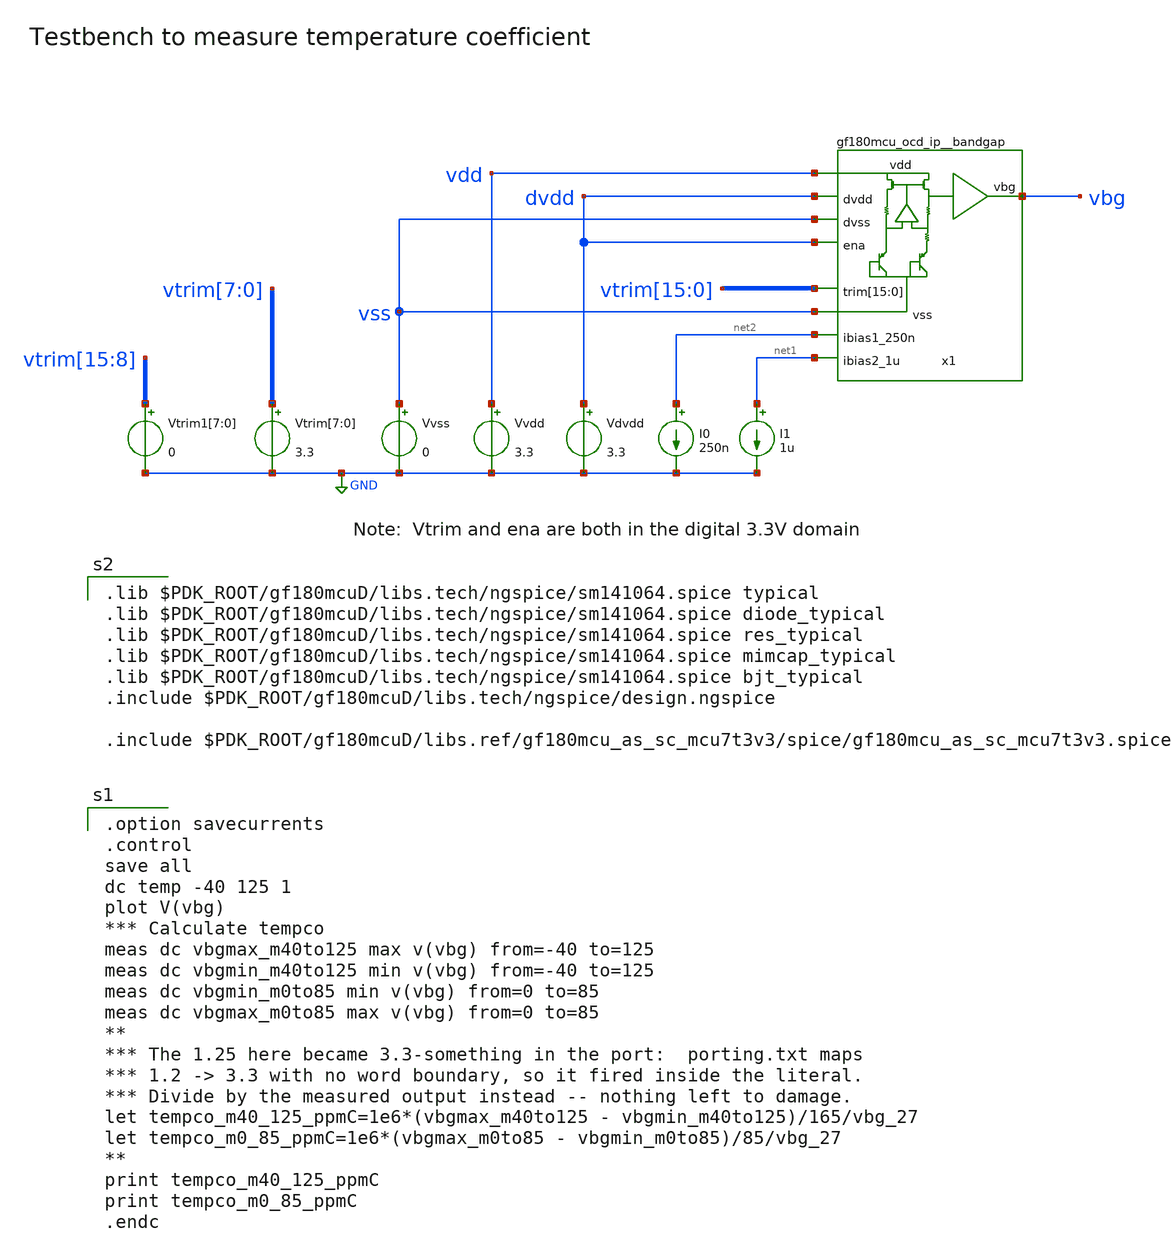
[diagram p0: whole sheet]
** sch_path: xschem/bandgap_tc_tb.sch
**.subckt bandgap_tc_tb
Vvss vss GND 0
Vtrim[7] vtrim[7] GND 3.3
Vtrim[6] vtrim[6] GND 3.3
Vtrim[5] vtrim[5] GND 3.3
Vtrim[4] vtrim[4] GND 3.3
Vtrim[3] vtrim[3] GND 3.3
Vtrim[2] vtrim[2] GND 3.3
Vtrim[1] vtrim[1] GND 3.3
Vtrim[0] vtrim[0] GND 3.3
Vvdd vdd GND 3.3
I0 net2 GND 250n
Vdvdd dvdd GND 3.3
I1 net1 GND 1u
Vtrim1[7] vtrim[15] GND 0
Vtrim1[6] vtrim[14] GND 0
Vtrim1[5] vtrim[13] GND 0
Vtrim1[4] vtrim[12] GND 0
Vtrim1[3] vtrim[11] GND 0
Vtrim1[2] vtrim[10] GND 0
Vtrim1[1] vtrim[9] GND 0
Vtrim1[0] vtrim[8] GND 0
x1 vdd vbg vss net2 vtrim[15] vtrim[14] vtrim[13] vtrim[12] vtrim[11] vtrim[10] vtrim[9] vtrim[8]
+ vtrim[7] vtrim[6] vtrim[5] vtrim[4] vtrim[3] vtrim[2] vtrim[1] vtrim[0] vss dvdd dvdd net1
+ gf180mcu_ocd_ip__bandgap
**** begin user architecture code

.option savecurrents
.control
save all
dc temp -40 125 1
plot V(vbg)
*** Calculate tempco
meas dc vbgmax_m40to125 max v(vbg) from=-40 to=125
meas dc vbgmin_m40to125 min v(vbg) from=-40 to=125
meas dc vbgmin_m0to85 min v(vbg) from=0 to=85
meas dc vbgmax_m0to85 max v(vbg) from=0 to=85
**
*** The 1.25 here became 3.3-something in the port:  porting.txt maps
*** 1.2 -> 3.3 with no word boundary, so it fired inside the literal.
*** Divide by the measured output instead -- nothing left to damage.
let tempco_m40_125_ppmC=1e6*(vbgmax_m40to125 - vbgmin_m40to125)/165/vbg_27
let tempco_m0_85_ppmC=1e6*(vbgmax_m0to85 - vbgmin_m0to85)/85/vbg_27
**
print tempco_m40_125_ppmC
print tempco_m0_85_ppmC
.endc


.lib $PDK_ROOT/gf180mcuD/libs.tech/ngspice/sm141064.spice typical
.lib $PDK_ROOT/gf180mcuD/libs.tech/ngspice/sm141064.spice diode_typical
.lib $PDK_ROOT/gf180mcuD/libs.tech/ngspice/sm141064.spice res_typical
.lib $PDK_ROOT/gf180mcuD/libs.tech/ngspice/sm141064.spice mimcap_typical
.lib $PDK_ROOT/gf180mcuD/libs.tech/ngspice/sm141064.spice bjt_typical
.include $PDK_ROOT/gf180mcuD/libs.tech/ngspice/design.ngspice

.include $PDK_ROOT/gf180mcuD/libs.ref/gf180mcu_as_sc_mcu7t3v3/spice/gf180mcu_as_sc_mcu7t3v3.spice


**** end user architecture code
**.ends
.GLOBAL GND
.end
